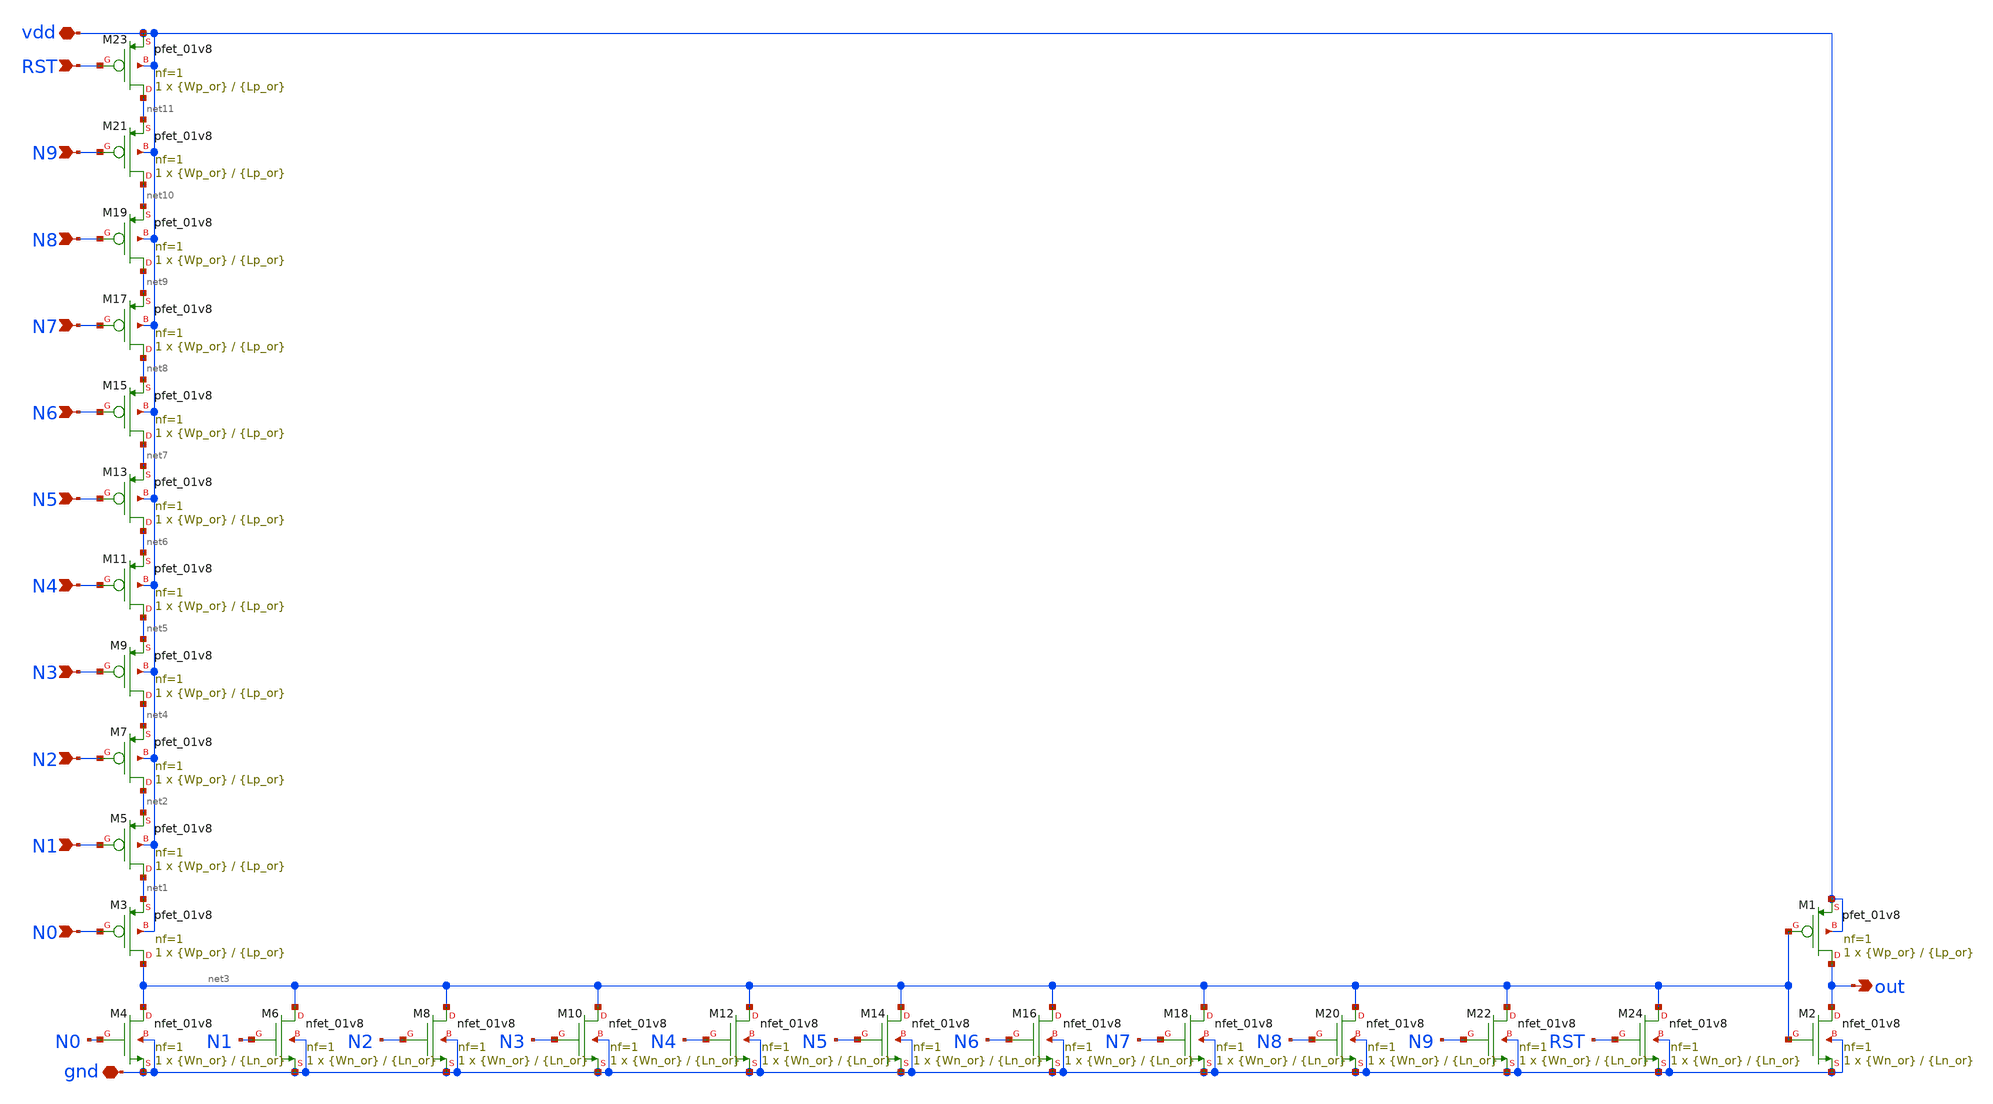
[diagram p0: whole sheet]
** sch_path: SNN/WTA_circuit.sch
**.subckt WTA_circuit gnd N0 N1 out vdd N2 N3 N4 N5 N6 N7 N8 N9 RST
*.iopin gnd
*.ipin N0
*.ipin N1
*.opin out
*.iopin vdd
*.ipin N2
*.ipin N3
*.ipin N4
*.ipin N5
*.ipin N6
*.ipin N7
*.ipin N8
*.ipin N9
*.ipin RST
XM5 net1 N1 net2 vdd sky130_fd_pr__pfet_01v8 L={Lp_or} W={Wp_or} nf=1 ad='int((nf+1)/2) * W/nf * 0.29'
+ as='int((nf+2)/2) * W/nf * 0.29' pd='2*int((nf+1)/2) * (W/nf + 0.29)' ps='2*int((nf+2)/2) * (W/nf + 0.29)'
+ nrd='0.29 / W' nrs='0.29 / W' sa=0 sb=0 sd=0 mult=1 m=1
XM6 net3 N1 gnd gnd sky130_fd_pr__nfet_01v8 L={Ln_or} W={Wn_or} nf=1 ad='int((nf+1)/2) * W/nf * 0.29'
+ as='int((nf+2)/2) * W/nf * 0.29' pd='2*int((nf+1)/2) * (W/nf + 0.29)' ps='2*int((nf+2)/2) * (W/nf + 0.29)'
+ nrd='0.29 / W' nrs='0.29 / W' sa=0 sb=0 sd=0 mult=1 m=1
XM3 net3 N0 net1 vdd sky130_fd_pr__pfet_01v8 L={Lp_or} W={Wp_or} nf=1 ad='int((nf+1)/2) * W/nf * 0.29'
+ as='int((nf+2)/2) * W/nf * 0.29' pd='2*int((nf+1)/2) * (W/nf + 0.29)' ps='2*int((nf+2)/2) * (W/nf + 0.29)'
+ nrd='0.29 / W' nrs='0.29 / W' sa=0 sb=0 sd=0 mult=1 m=1
XM4 net3 N0 gnd gnd sky130_fd_pr__nfet_01v8 L={Ln_or} W={Wn_or} nf=1 ad='int((nf+1)/2) * W/nf * 0.29'
+ as='int((nf+2)/2) * W/nf * 0.29' pd='2*int((nf+1)/2) * (W/nf + 0.29)' ps='2*int((nf+2)/2) * (W/nf + 0.29)'
+ nrd='0.29 / W' nrs='0.29 / W' sa=0 sb=0 sd=0 mult=1 m=1
XM2 out net3 gnd gnd sky130_fd_pr__nfet_01v8 L={Ln_or} W={Wn_or} nf=1 ad='int((nf+1)/2) * W/nf * 0.29'
+ as='int((nf+2)/2) * W/nf * 0.29' pd='2*int((nf+1)/2) * (W/nf + 0.29)' ps='2*int((nf+2)/2) * (W/nf + 0.29)'
+ nrd='0.29 / W' nrs='0.29 / W' sa=0 sb=0 sd=0 mult=1 m=1
XM1 out net3 vdd vdd sky130_fd_pr__pfet_01v8 L={Lp_or} W={Wp_or} nf=1 ad='int((nf+1)/2) * W/nf * 0.29'
+ as='int((nf+2)/2) * W/nf * 0.29' pd='2*int((nf+1)/2) * (W/nf + 0.29)' ps='2*int((nf+2)/2) * (W/nf + 0.29)'
+ nrd='0.29 / W' nrs='0.29 / W' sa=0 sb=0 sd=0 mult=1 m=1
XM7 net2 N2 net4 vdd sky130_fd_pr__pfet_01v8 L={Lp_or} W={Wp_or} nf=1 ad='int((nf+1)/2) * W/nf * 0.29'
+ as='int((nf+2)/2) * W/nf * 0.29' pd='2*int((nf+1)/2) * (W/nf + 0.29)' ps='2*int((nf+2)/2) * (W/nf + 0.29)'
+ nrd='0.29 / W' nrs='0.29 / W' sa=0 sb=0 sd=0 mult=1 m=1
XM8 net3 N2 gnd gnd sky130_fd_pr__nfet_01v8 L={Ln_or} W={Wn_or} nf=1 ad='int((nf+1)/2) * W/nf * 0.29'
+ as='int((nf+2)/2) * W/nf * 0.29' pd='2*int((nf+1)/2) * (W/nf + 0.29)' ps='2*int((nf+2)/2) * (W/nf + 0.29)'
+ nrd='0.29 / W' nrs='0.29 / W' sa=0 sb=0 sd=0 mult=1 m=1
XM9 net4 N3 net5 vdd sky130_fd_pr__pfet_01v8 L={Lp_or} W={Wp_or} nf=1 ad='int((nf+1)/2) * W/nf * 0.29'
+ as='int((nf+2)/2) * W/nf * 0.29' pd='2*int((nf+1)/2) * (W/nf + 0.29)' ps='2*int((nf+2)/2) * (W/nf + 0.29)'
+ nrd='0.29 / W' nrs='0.29 / W' sa=0 sb=0 sd=0 mult=1 m=1
XM11 net5 N4 net6 vdd sky130_fd_pr__pfet_01v8 L={Lp_or} W={Wp_or} nf=1 ad='int((nf+1)/2) * W/nf * 0.29'
+ as='int((nf+2)/2) * W/nf * 0.29' pd='2*int((nf+1)/2) * (W/nf + 0.29)' ps='2*int((nf+2)/2) * (W/nf + 0.29)'
+ nrd='0.29 / W' nrs='0.29 / W' sa=0 sb=0 sd=0 mult=1 m=1
XM13 net6 N5 net7 vdd sky130_fd_pr__pfet_01v8 L={Lp_or} W={Wp_or} nf=1 ad='int((nf+1)/2) * W/nf * 0.29'
+ as='int((nf+2)/2) * W/nf * 0.29' pd='2*int((nf+1)/2) * (W/nf + 0.29)' ps='2*int((nf+2)/2) * (W/nf + 0.29)'
+ nrd='0.29 / W' nrs='0.29 / W' sa=0 sb=0 sd=0 mult=1 m=1
XM15 net7 N6 net8 vdd sky130_fd_pr__pfet_01v8 L={Lp_or} W={Wp_or} nf=1 ad='int((nf+1)/2) * W/nf * 0.29'
+ as='int((nf+2)/2) * W/nf * 0.29' pd='2*int((nf+1)/2) * (W/nf + 0.29)' ps='2*int((nf+2)/2) * (W/nf + 0.29)'
+ nrd='0.29 / W' nrs='0.29 / W' sa=0 sb=0 sd=0 mult=1 m=1
XM17 net8 N7 net9 vdd sky130_fd_pr__pfet_01v8 L={Lp_or} W={Wp_or} nf=1 ad='int((nf+1)/2) * W/nf * 0.29'
+ as='int((nf+2)/2) * W/nf * 0.29' pd='2*int((nf+1)/2) * (W/nf + 0.29)' ps='2*int((nf+2)/2) * (W/nf + 0.29)'
+ nrd='0.29 / W' nrs='0.29 / W' sa=0 sb=0 sd=0 mult=1 m=1
XM19 net9 N8 net10 vdd sky130_fd_pr__pfet_01v8 L={Lp_or} W={Wp_or} nf=1 ad='int((nf+1)/2) * W/nf * 0.29'
+ as='int((nf+2)/2) * W/nf * 0.29' pd='2*int((nf+1)/2) * (W/nf + 0.29)' ps='2*int((nf+2)/2) * (W/nf + 0.29)'
+ nrd='0.29 / W' nrs='0.29 / W' sa=0 sb=0 sd=0 mult=1 m=1
XM21 net10 N9 net11 vdd sky130_fd_pr__pfet_01v8 L={Lp_or} W={Wp_or} nf=1 ad='int((nf+1)/2) * W/nf * 0.29'
+ as='int((nf+2)/2) * W/nf * 0.29' pd='2*int((nf+1)/2) * (W/nf + 0.29)' ps='2*int((nf+2)/2) * (W/nf + 0.29)'
+ nrd='0.29 / W' nrs='0.29 / W' sa=0 sb=0 sd=0 mult=1 m=1
XM10 net3 N3 gnd gnd sky130_fd_pr__nfet_01v8 L={Ln_or} W={Wn_or} nf=1 ad='int((nf+1)/2) * W/nf * 0.29'
+ as='int((nf+2)/2) * W/nf * 0.29' pd='2*int((nf+1)/2) * (W/nf + 0.29)' ps='2*int((nf+2)/2) * (W/nf + 0.29)'
+ nrd='0.29 / W' nrs='0.29 / W' sa=0 sb=0 sd=0 mult=1 m=1
XM12 net3 N4 gnd gnd sky130_fd_pr__nfet_01v8 L={Ln_or} W={Wn_or} nf=1 ad='int((nf+1)/2) * W/nf * 0.29'
+ as='int((nf+2)/2) * W/nf * 0.29' pd='2*int((nf+1)/2) * (W/nf + 0.29)' ps='2*int((nf+2)/2) * (W/nf + 0.29)'
+ nrd='0.29 / W' nrs='0.29 / W' sa=0 sb=0 sd=0 mult=1 m=1
XM14 net3 N5 gnd gnd sky130_fd_pr__nfet_01v8 L={Ln_or} W={Wn_or} nf=1 ad='int((nf+1)/2) * W/nf * 0.29'
+ as='int((nf+2)/2) * W/nf * 0.29' pd='2*int((nf+1)/2) * (W/nf + 0.29)' ps='2*int((nf+2)/2) * (W/nf + 0.29)'
+ nrd='0.29 / W' nrs='0.29 / W' sa=0 sb=0 sd=0 mult=1 m=1
XM16 net3 N6 gnd gnd sky130_fd_pr__nfet_01v8 L={Ln_or} W={Wn_or} nf=1 ad='int((nf+1)/2) * W/nf * 0.29'
+ as='int((nf+2)/2) * W/nf * 0.29' pd='2*int((nf+1)/2) * (W/nf + 0.29)' ps='2*int((nf+2)/2) * (W/nf + 0.29)'
+ nrd='0.29 / W' nrs='0.29 / W' sa=0 sb=0 sd=0 mult=1 m=1
XM18 net3 N7 gnd gnd sky130_fd_pr__nfet_01v8 L={Ln_or} W={Wn_or} nf=1 ad='int((nf+1)/2) * W/nf * 0.29'
+ as='int((nf+2)/2) * W/nf * 0.29' pd='2*int((nf+1)/2) * (W/nf + 0.29)' ps='2*int((nf+2)/2) * (W/nf + 0.29)'
+ nrd='0.29 / W' nrs='0.29 / W' sa=0 sb=0 sd=0 mult=1 m=1
XM20 net3 N8 gnd gnd sky130_fd_pr__nfet_01v8 L={Ln_or} W={Wn_or} nf=1 ad='int((nf+1)/2) * W/nf * 0.29'
+ as='int((nf+2)/2) * W/nf * 0.29' pd='2*int((nf+1)/2) * (W/nf + 0.29)' ps='2*int((nf+2)/2) * (W/nf + 0.29)'
+ nrd='0.29 / W' nrs='0.29 / W' sa=0 sb=0 sd=0 mult=1 m=1
XM22 net3 N9 gnd gnd sky130_fd_pr__nfet_01v8 L={Ln_or} W={Wn_or} nf=1 ad='int((nf+1)/2) * W/nf * 0.29'
+ as='int((nf+2)/2) * W/nf * 0.29' pd='2*int((nf+1)/2) * (W/nf + 0.29)' ps='2*int((nf+2)/2) * (W/nf + 0.29)'
+ nrd='0.29 / W' nrs='0.29 / W' sa=0 sb=0 sd=0 mult=1 m=1
XM23 net11 RST vdd vdd sky130_fd_pr__pfet_01v8 L={Lp_or} W={Wp_or} nf=1 ad='int((nf+1)/2) * W/nf * 0.29'
+ as='int((nf+2)/2) * W/nf * 0.29' pd='2*int((nf+1)/2) * (W/nf + 0.29)' ps='2*int((nf+2)/2) * (W/nf + 0.29)'
+ nrd='0.29 / W' nrs='0.29 / W' sa=0 sb=0 sd=0 mult=1 m=1
XM24 net3 RST gnd gnd sky130_fd_pr__nfet_01v8 L={Ln_or} W={Wn_or} nf=1 ad='int((nf+1)/2) * W/nf * 0.29'
+ as='int((nf+2)/2) * W/nf * 0.29' pd='2*int((nf+1)/2) * (W/nf + 0.29)' ps='2*int((nf+2)/2) * (W/nf + 0.29)'
+ nrd='0.29 / W' nrs='0.29 / W' sa=0 sb=0 sd=0 mult=1 m=1
**.ends
.end
